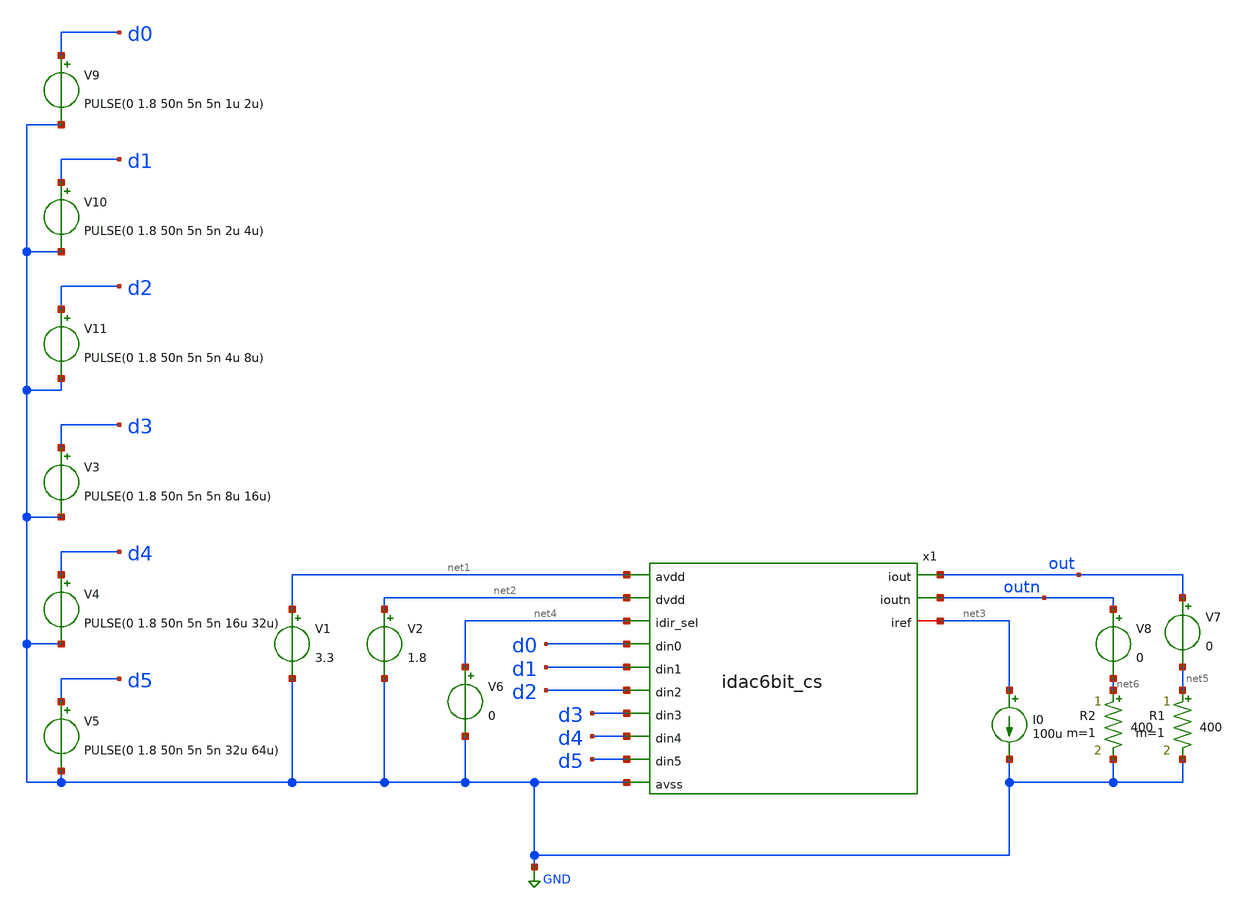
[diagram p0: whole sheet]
** sch_path: xschem/idac6bit_cs_tb.sch
**.subckt idac6bit_cs_tb
V1 net1 GND 3.3
V2 net2 GND 1.8
I0 net3 GND 100u
V3 d3 GND PULSE(0 1.8 50n 5n 5n 8u 16u)
V4 d4 GND PULSE(0 1.8 50n 5n 5n 16u 32u)
V5 d5 GND PULSE(0 1.8 50n 5n 5n 32u 64u)
V6 net4 GND 0
V7 out net5 0
R1 net5 GND 400 m=1
V8 outn net6 0
R2 net6 GND 400 m=1
V9 d0 GND PULSE(0 1.8 50n 5n 5n 1u 2u)
V10 d1 GND PULSE(0 1.8 50n 5n 5n 2u 4u)
V11 d2 GND PULSE(0 1.8 50n 5n 5n 4u 8u)
x1 net1 net2 out outn d0 net4 d1 GND d2 d3 net3 d4 d5 idac6bit_cs
**** begin user architecture code
 .lib $::SKYWATER_MODELS/sky130.lib.spice tt
.include $::SKYWATER_STDCELLS/../../sky130_fd_sc_hvl/spice/sky130_fd_sc_hvl.spice

.param mc_mm_switch=0
.param mc_pr_switch=1



.option wnflag=0
.option savecurrents
.control
save all
tran 100n 64u
plot v(out) v(outn)
write currentmirrortb.raw
op
.endc


**** end user architecture code
**.ends
.GLOBAL GND
.end
